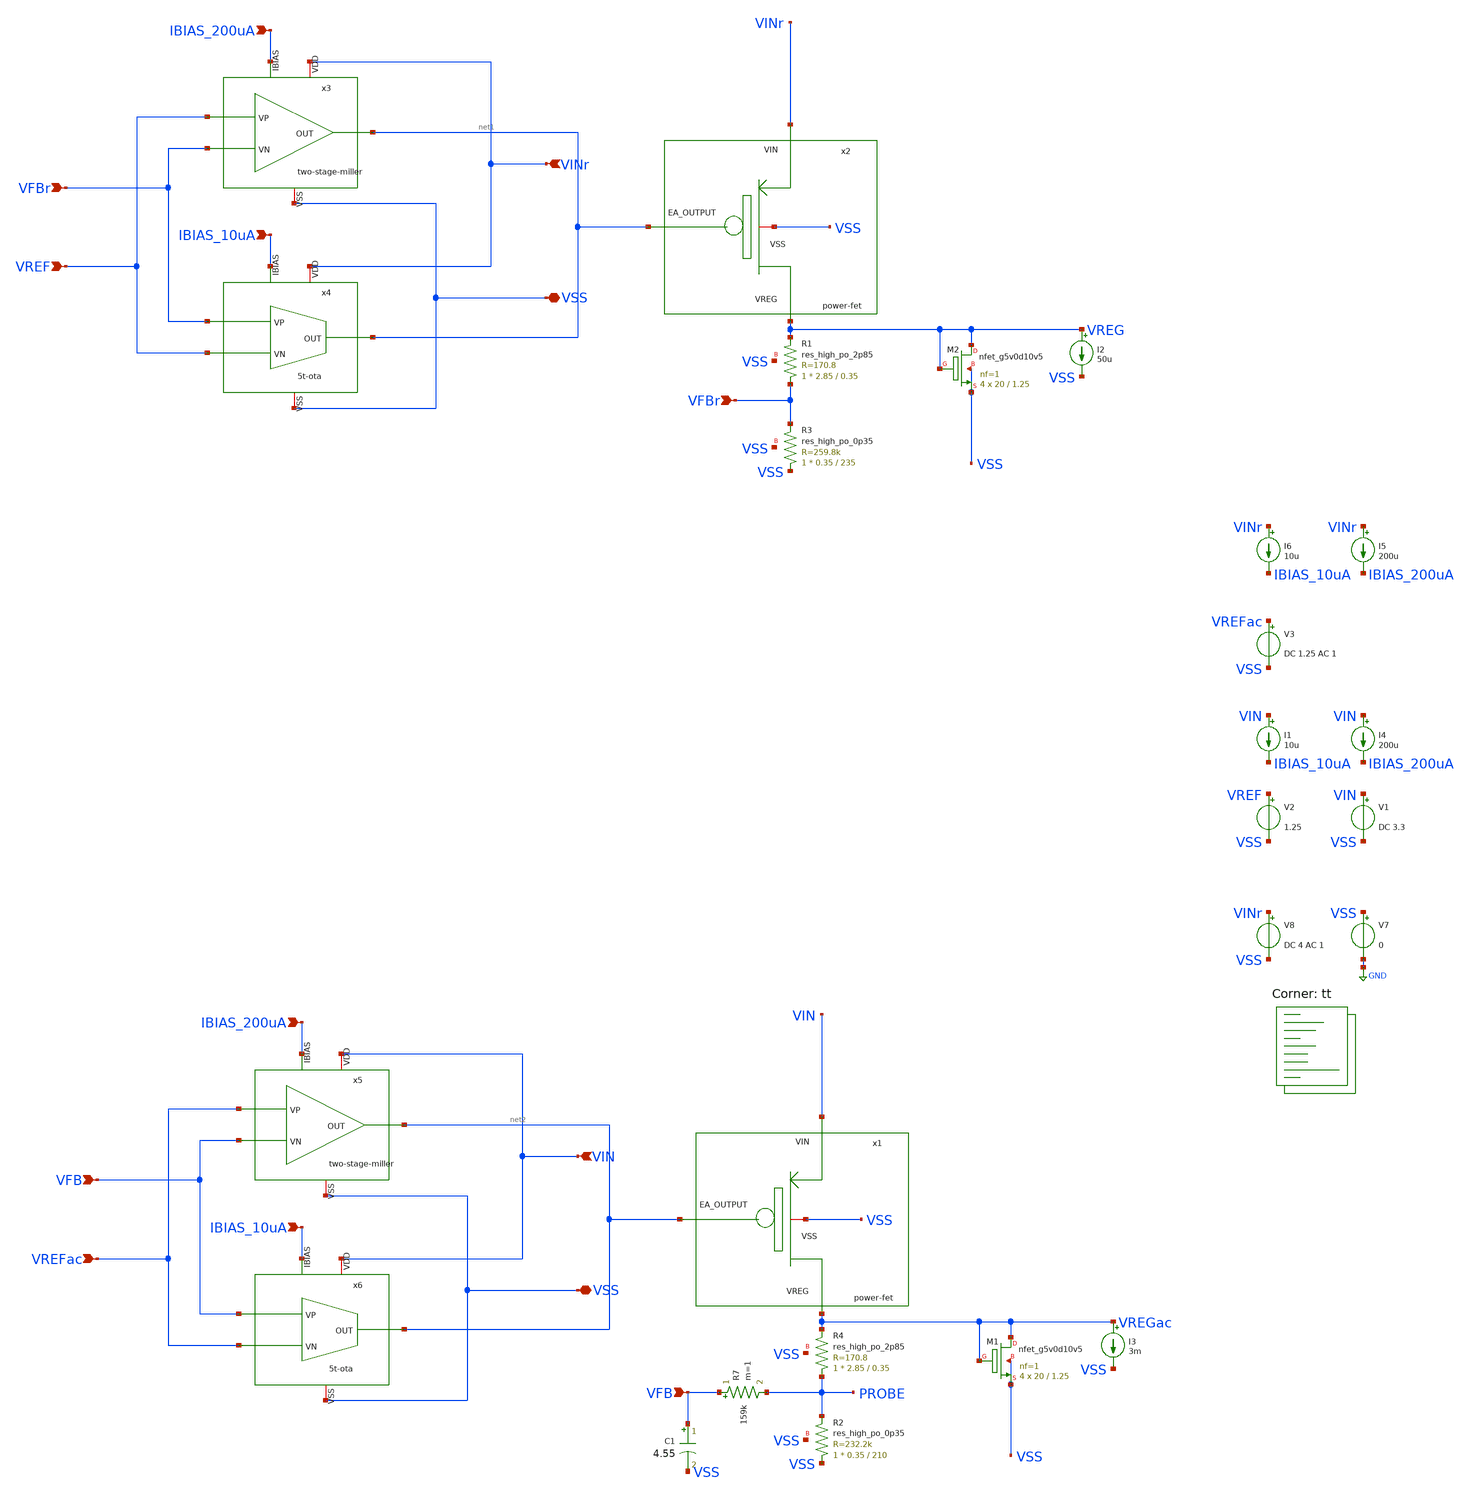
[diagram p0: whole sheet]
** sch_path: xschem/ldo-core/testing/ldo_ac_standalone.sch
**.subckt ldo_ac_standalone VFBr VFBr VREF IBIAS_10uA IBIAS_200uA VINr VSS VFB VREFac IBIAS_10uA
*+ IBIAS_200uA VIN VSS VFB
*.ipin VFBr
*.ipin VFBr
*.ipin VREF
*.ipin IBIAS_10uA
*.ipin IBIAS_200uA
*.ipin VINr
*.iopin VSS
*.ipin VFB
*.ipin VREFac
*.ipin IBIAS_10uA
*.ipin IBIAS_200uA
*.ipin VIN
*.iopin VSS
*.ipin VFB
x2 VINr VSS net1 VREG power-fet
XR3 VSS VFBr VSS sky130_fd_pr__res_high_po_0p35 L=235 mult=1 m=1
XR1 VFBr VREG VSS sky130_fd_pr__res_high_po_2p85 L=0.35 mult=1 m=1
x3 VINr net1 VREF VFBr IBIAS_200uA VSS two-stage-miller
x4 VINr net1 IBIAS_10uA VREF VFBr VSS 5t-ota
I2 VREG VSS 50u
V2 VREF VSS 1.25
V7 VSS GND 0
V8 VINr VSS DC 4 AC 1
I4 VIN IBIAS_200uA 200u
I1 VIN IBIAS_10uA 10u
x1 VIN VSS net2 VREGac power-fet
XR4 PROBE VREGac VSS sky130_fd_pr__res_high_po_2p85 L=0.35 mult=1 m=1
x5 VIN net2 VREFac VFB IBIAS_200uA VSS two-stage-miller
x6 VIN net2 IBIAS_10uA VREFac VFB VSS 5t-ota
I3 VREGac VSS 3m
V1 VIN VSS DC 3.3
XR2 VSS PROBE VSS sky130_fd_pr__res_high_po_0p35 L=210 mult=1 m=1
R7 VFB PROBE 159k m=1
C1 VFB VSS 4.55 m=1
V3 VREFac VSS DC 1.25 AC 1
XM2 VREG VREG VSS VSS sky130_fd_pr__nfet_g5v0d10v5 L=1.25 W=20 nf=1 ad='int((nf+1)/2) * W/nf * 0.29'
+ as='int((nf+2)/2) * W/nf * 0.29' pd='2*int((nf+1)/2) * (W/nf + 0.29)' ps='2*int((nf+2)/2) * (W/nf + 0.29)'
+ nrd='0.29 / W' nrs='0.29 / W' sa=0 sb=0 sd=0 mult=4 m=4
XM1 VREGac VREGac VSS VSS sky130_fd_pr__nfet_g5v0d10v5 L=1.25 W=20 nf=1 ad='int((nf+1)/2) * W/nf * 0.29'
+ as='int((nf+2)/2) * W/nf * 0.29' pd='2*int((nf+1)/2) * (W/nf + 0.29)' ps='2*int((nf+2)/2) * (W/nf + 0.29)'
+ nrd='0.29 / W' nrs='0.29 / W' sa=0 sb=0 sd=0 mult=4 m=4
I5 VINr IBIAS_200uA 200u
I6 VINr IBIAS_10uA 10u
**** begin user architecture code



.temp 27
.control

AC DEC 100 1 100G
let PSRR = -20*log10(VREG)
* Phase (same expression form you used — adopted)
let phase = 180 + 180*cph( v(VREGac) )/pi

* 1. Calculate the True Loop Gain (T)
  * T = V_return / V_injected
  let loop_gain_complex = v(PROBE)
  let lg_db = db(loop_gain_complex)
  let lg_ph = ph(loop_gain_complex) * 180 / PI

* 2. Normalize Phase (so it starts at 0 or 180 depending on your EA polarity)
  * For a standard LDO, we want to see how far we are from -180 degrees.
  let phase_margin_plot = lg_ph + 180

* 3. Automatically find the Phase Margin value
  meas ac f_unity when lg_db=0
  meas ac PM_value find phase_margin_plot when frequency=f_unity

  echo Unity Gain Frequency: $&f_unity Hz
  echo Phase Margin: $&PM_value degrees

  plot lg_db
  plot lg_db phase_margin_plot


	plot PSRR
	plot phase

.endc


.lib $::SKYWATER_MODELS/sky130.lib.spice tt
**** end user architecture code
**.ends
.GLOBAL GND
.end
